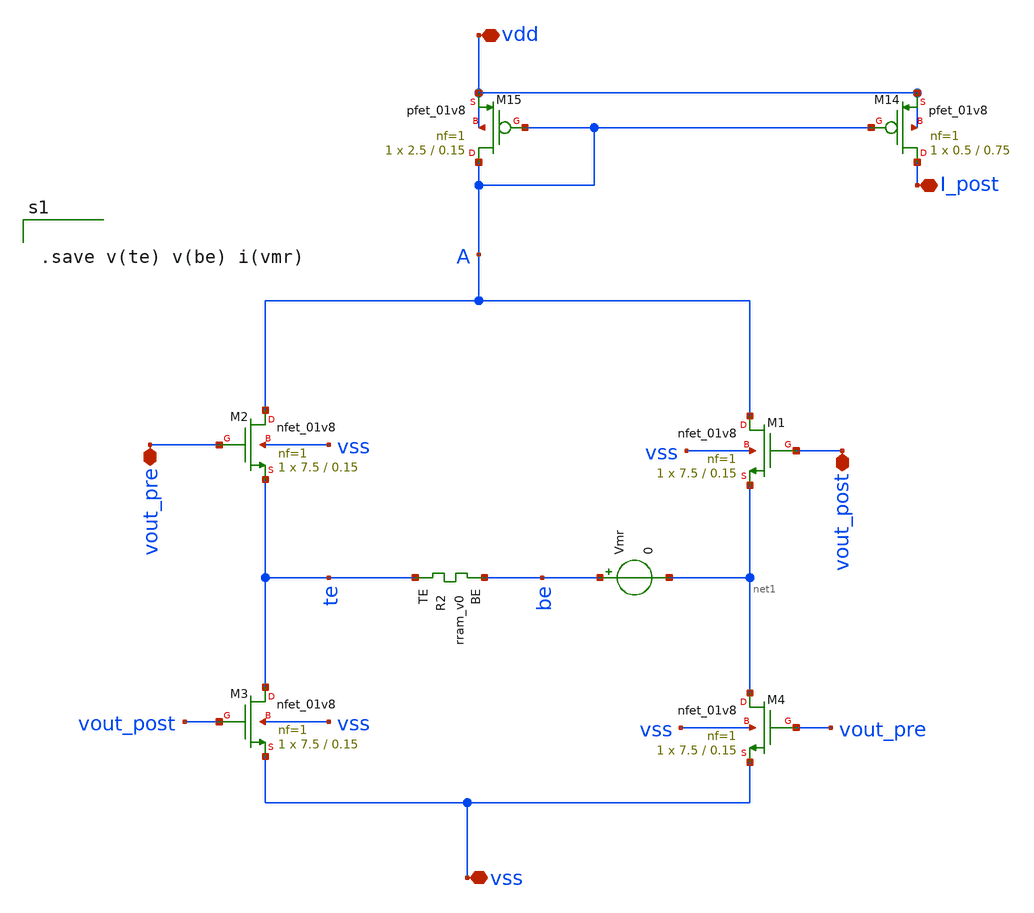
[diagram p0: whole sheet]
** sch_path: Synapse/stdp.sch
**.subckt stdp vdd vss vout_post vout_pre I_post
*.iopin vdd
*.iopin vss
*.iopin vout_post
*.iopin vout_pre
*.iopin I_post
XM2 A vout_pre te vss sky130_fd_pr__nfet_01v8 L=0.15 W=7.5 nf=1 ad='int((nf+1)/2) * W/nf * 0.29' as='int((nf+2)/2) * W/nf * 0.29'
+ pd='2*int((nf+1)/2) * (W/nf + 0.29)' ps='2*int((nf+2)/2) * (W/nf + 0.29)' nrd='0.29 / W' nrs='0.29 / W'
+ sa=0 sb=0 sd=0 mult=1 m=1
XM3 te vout_post vss vss sky130_fd_pr__nfet_01v8 L=0.15 W=7.5 nf=1 ad='int((nf+1)/2) * W/nf * 0.29' as='int((nf+2)/2) * W/nf * 0.29'
+ pd='2*int((nf+1)/2) * (W/nf + 0.29)' ps='2*int((nf+2)/2) * (W/nf + 0.29)' nrd='0.29 / W' nrs='0.29 / W'
+ sa=0 sb=0 sd=0 mult=1 m=1
XM1 A vout_post net1 vss sky130_fd_pr__nfet_01v8 L=0.15 W=7.5 nf=1 ad='int((nf+1)/2) * W/nf * 0.29' as='int((nf+2)/2) * W/nf * 0.29'
+ pd='2*int((nf+1)/2) * (W/nf + 0.29)' ps='2*int((nf+2)/2) * (W/nf + 0.29)' nrd='0.29 / W' nrs='0.29 / W'
+ sa=0 sb=0 sd=0 mult=1 m=1
XM4 net1 vout_pre vss vss sky130_fd_pr__nfet_01v8 L=0.15 W=7.5 nf=1 ad='int((nf+1)/2) * W/nf * 0.29'
+ as='int((nf+2)/2) * W/nf * 0.29' pd='2*int((nf+1)/2) * (W/nf + 0.29)' ps='2*int((nf+2)/2) * (W/nf + 0.29)'
+ nrd='0.29 / W' nrs='0.29 / W' sa=0 sb=0 sd=0 mult=1 m=1
XR2 te be rram_v0
XM14 I_post A vdd vdd sky130_fd_pr__pfet_01v8 L=0.75 W=0.5 nf=1 ad='int((nf+1)/2) * W/nf * 0.29' as='int((nf+2)/2) * W/nf * 0.29'
+ pd='2*int((nf+1)/2) * (W/nf + 0.29)' ps='2*int((nf+2)/2) * (W/nf + 0.29)' nrd='0.29 / W' nrs='0.29 / W'
+ sa=0 sb=0 sd=0 mult=1 m=1
XM15 A A vdd vdd sky130_fd_pr__pfet_01v8 L=0.15 W=2.5 nf=1 ad='int((nf+1)/2) * W/nf * 0.29' as='int((nf+2)/2) * W/nf * 0.29'
+ pd='2*int((nf+1)/2) * (W/nf + 0.29)' ps='2*int((nf+2)/2) * (W/nf + 0.29)' nrd='0.29 / W' nrs='0.29 / W'
+ sa=0 sb=0 sd=0 mult=1 m=1
Vmr be net1 0
.save i(vmr)
**** begin user architecture code


.save v(te) v(be) i(vmr)


**** end user architecture code
**.ends
.end
